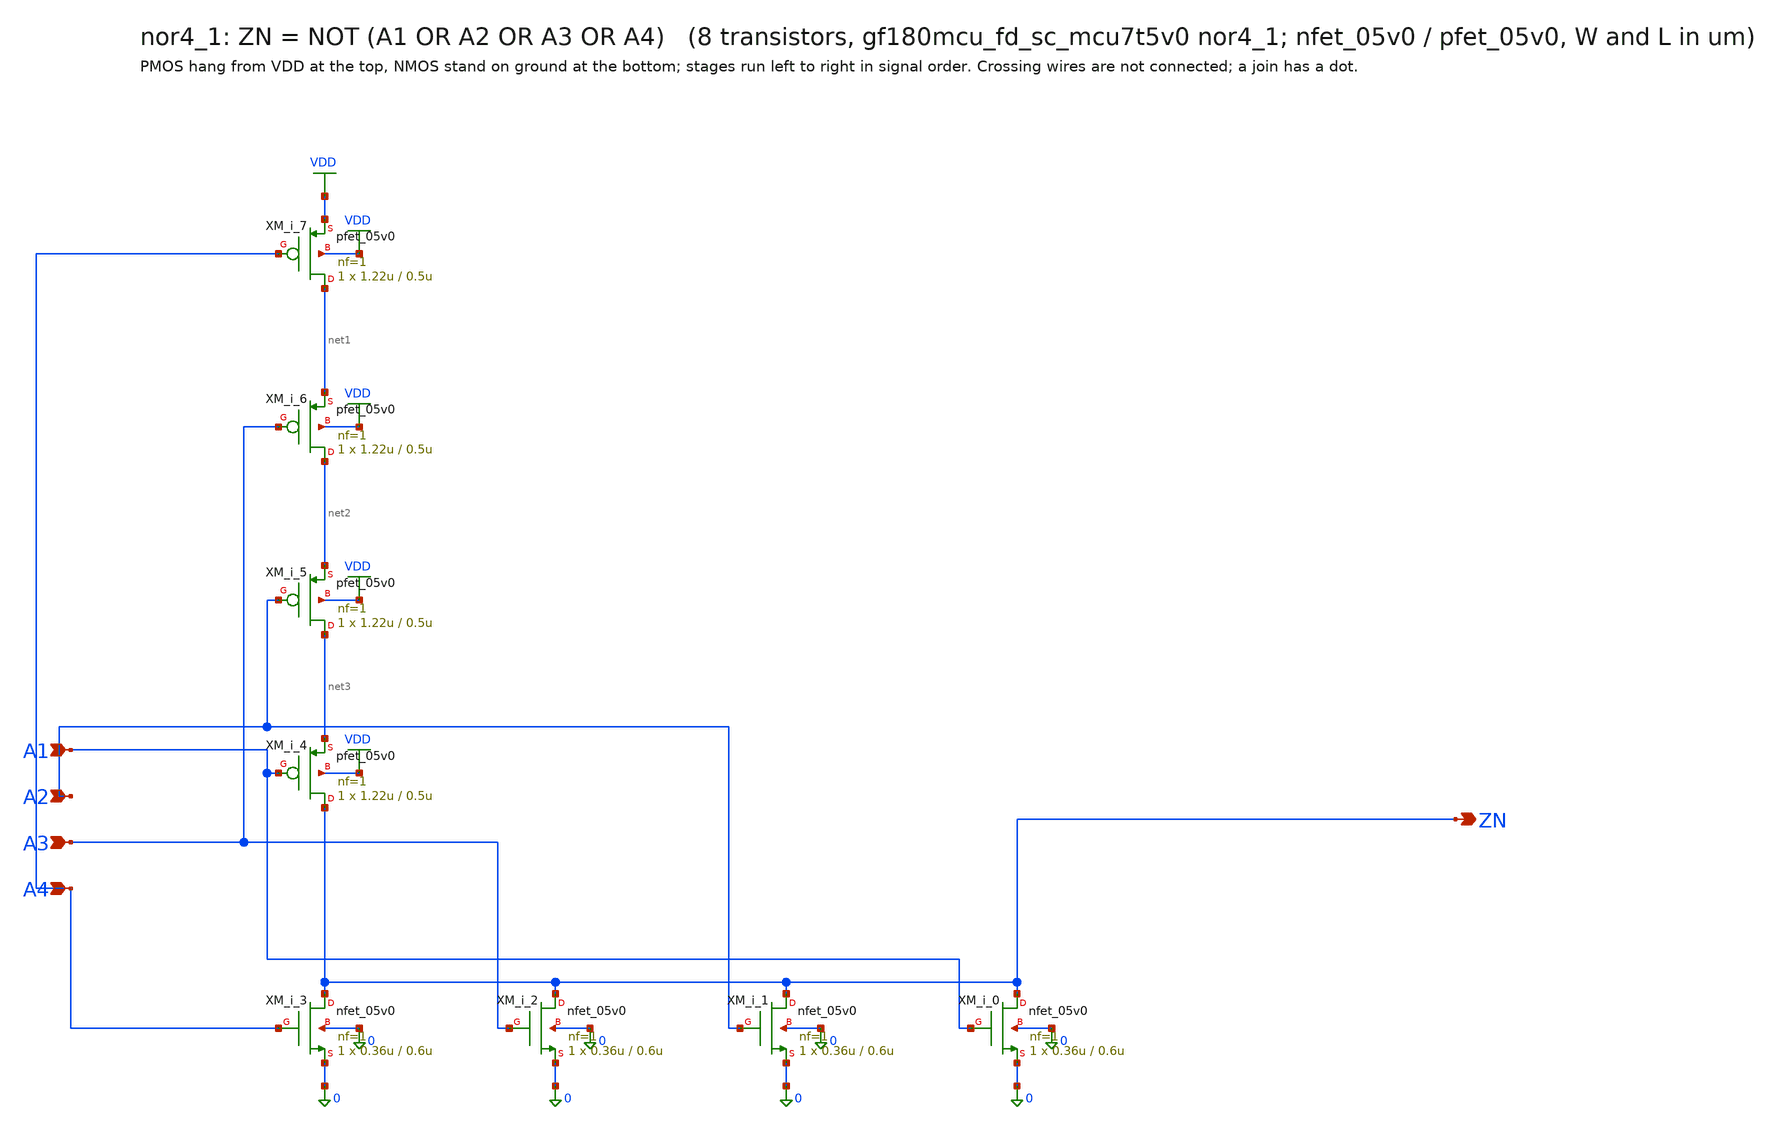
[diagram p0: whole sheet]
** sch_path: xschem/cells_tx/nor4_1.sch
**.subckt nor4_1 A1 A2 A3 A4 ZN
*.ipin A1
*.ipin A2
*.ipin A3
*.ipin A4
*.opin ZN
XM_i_3 ZN A4 0 0 nfet_05v0 L=0.6u W=0.36u nf=1 ad=1.8e-13 as=1.8e-13 pd=1.72e-06 ps=1.72e-06 nrd=0
+ nrs=0 sa=0 sb=0 sd=0 m=1
XM_i_2 ZN A3 0 0 nfet_05v0 L=0.6u W=0.36u nf=1 ad=1.8e-13 as=1.8e-13 pd=1.72e-06 ps=1.72e-06 nrd=0
+ nrs=0 sa=0 sb=0 sd=0 m=1
XM_i_1 ZN A2 0 0 nfet_05v0 L=0.6u W=0.36u nf=1 ad=1.8e-13 as=1.8e-13 pd=1.72e-06 ps=1.72e-06 nrd=0
+ nrs=0 sa=0 sb=0 sd=0 m=1
XM_i_0 ZN A1 0 0 nfet_05v0 L=0.6u W=0.36u nf=1 ad=1.8e-13 as=1.8e-13 pd=1.72e-06 ps=1.72e-06 nrd=0
+ nrs=0 sa=0 sb=0 sd=0 m=1
XM_i_7 net1 A4 VDD VDD pfet_05v0 L=0.5u W=1.22u nf=1 ad=6.1e-13 as=6.1e-13 pd=3.44e-06 ps=3.44e-06
+ nrd=0 nrs=0 sa=0 sb=0 sd=0 m=1
XM_i_6 net2 A3 net1 VDD pfet_05v0 L=0.5u W=1.22u nf=1 ad=6.1e-13 as=6.1e-13 pd=3.44e-06 ps=3.44e-06
+ nrd=0 nrs=0 sa=0 sb=0 sd=0 m=1
XM_i_5 net3 A2 net2 VDD pfet_05v0 L=0.5u W=1.22u nf=1 ad=6.1e-13 as=6.1e-13 pd=3.44e-06 ps=3.44e-06
+ nrd=0 nrs=0 sa=0 sb=0 sd=0 m=1
XM_i_4 ZN A1 net3 VDD pfet_05v0 L=0.5u W=1.22u nf=1 ad=6.1e-13 as=6.1e-13 pd=3.44e-06 ps=3.44e-06
+ nrd=0 nrs=0 sa=0 sb=0 sd=0 m=1
**.ends
.GLOBAL VDD
.end
